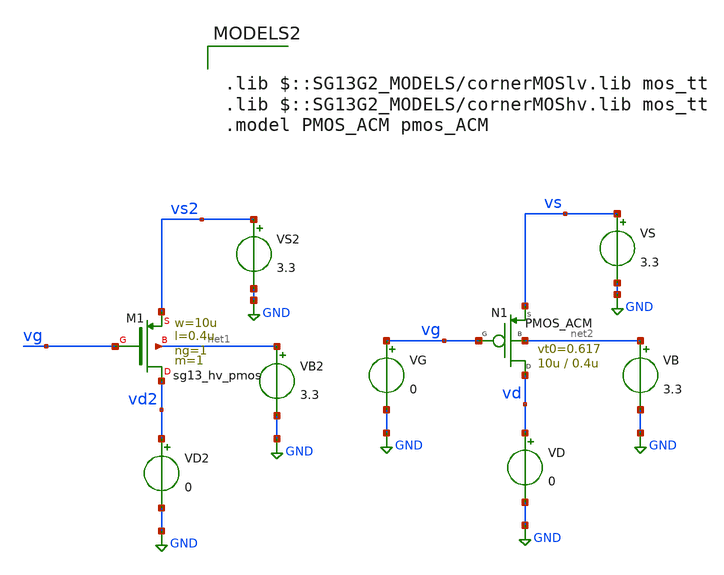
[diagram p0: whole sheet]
** sch_path: legacy/Examples/IHP-SG13/xschem/Extraction/TB_pmos_acm.sch
**.subckt TB_pmos_acm
VG vg GND 0
VS2 vs2 GND 3.3
VB2 net1 GND 3.3
VD2 vd2 GND 0
VS vs GND 3.3
VB net2 GND 3.3
VD vd GND 0
XM1 vd2 vg vs2 net1 sg13_hv_pmos w=10u l=0.4u ng=1 m=1 mm_ok=1
N1 vd vg vs net2 PMOS_ACM w=10u l=0.4u n=1.47 is=0.67u vt0=0.617 sigma=9m zeta=5.7m
**** begin user architecture code



.control
pre_osdi ./PMOS_ACM_2V0.osdi
pre_osdi ./psp103_nqs.osdi
ssave all

dc VG -0.05 3.3 5m


*gm for ACM
let gm_id = -deriv(ln(i(Vd)))

*gm for GF180
let gm_id_gf = -deriv(ln(i(Vd2)))

save gm_id gm_id_gf
write TB_pmos_acm.raw

.endc



.lib $::SG13G2_MODELS/cornerMOSlv.lib mos_tt
.lib $::SG13G2_MODELS/cornerMOShv.lib mos_tt
.model PMOS_ACM pmos_ACM

**** end user architecture code
**.ends
.GLOBAL GND
.end
